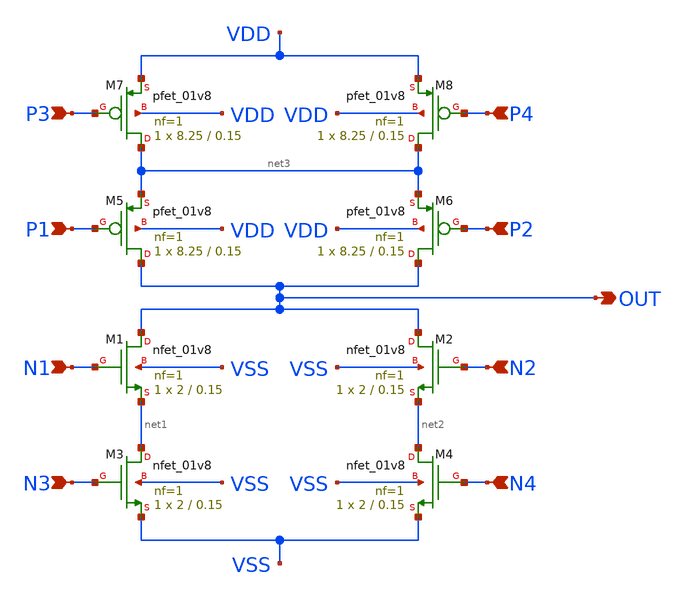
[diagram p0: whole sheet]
** sch_path: design/xschem/CG4/cg4.sch
**.subckt cg4 P3 P1 N1 N3 P4 P2 N2 N4 OUT
*.ipin P3
*.ipin P1
*.ipin N1
*.ipin N3
*.ipin P4
*.ipin P2
*.ipin N2
*.ipin N4
*.opin OUT
XM1 OUT N1 net1 VSS sky130_fd_pr__nfet_01v8 L=0.15 W=2 nf=1 ad='int((nf+1)/2) * W/nf * 0.29' as='int((nf+2)/2) * W/nf * 0.29'
+ pd='2*int((nf+1)/2) * (W/nf + 0.29)' ps='2*int((nf+2)/2) * (W/nf + 0.29)' nrd='0.29 / W' nrs='0.29 / W'
+ sa=0 sb=0 sd=0 mult=1 m=1
XM2 OUT N2 net2 VSS sky130_fd_pr__nfet_01v8 L=0.15 W=2 nf=1 ad='int((nf+1)/2) * W/nf * 0.29' as='int((nf+2)/2) * W/nf * 0.29'
+ pd='2*int((nf+1)/2) * (W/nf + 0.29)' ps='2*int((nf+2)/2) * (W/nf + 0.29)' nrd='0.29 / W' nrs='0.29 / W'
+ sa=0 sb=0 sd=0 mult=1 m=1
XM3 net1 N3 VSS VSS sky130_fd_pr__nfet_01v8 L=0.15 W=2 nf=1 ad='int((nf+1)/2) * W/nf * 0.29' as='int((nf+2)/2) * W/nf * 0.29'
+ pd='2*int((nf+1)/2) * (W/nf + 0.29)' ps='2*int((nf+2)/2) * (W/nf + 0.29)' nrd='0.29 / W' nrs='0.29 / W'
+ sa=0 sb=0 sd=0 mult=1 m=1
XM4 net2 N4 VSS VSS sky130_fd_pr__nfet_01v8 L=0.15 W=2 nf=1 ad='int((nf+1)/2) * W/nf * 0.29' as='int((nf+2)/2) * W/nf * 0.29'
+ pd='2*int((nf+1)/2) * (W/nf + 0.29)' ps='2*int((nf+2)/2) * (W/nf + 0.29)' nrd='0.29 / W' nrs='0.29 / W'
+ sa=0 sb=0 sd=0 mult=1 m=1
XM5 OUT P1 net3 VDD sky130_fd_pr__pfet_01v8 L=0.15 W=8.25 nf=1 ad='int((nf+1)/2) * W/nf * 0.29' as='int((nf+2)/2) * W/nf * 0.29'
+ pd='2*int((nf+1)/2) * (W/nf + 0.29)' ps='2*int((nf+2)/2) * (W/nf + 0.29)' nrd='0.29 / W' nrs='0.29 / W'
+ sa=0 sb=0 sd=0 mult=1 m=1
XM6 OUT P2 net3 VDD sky130_fd_pr__pfet_01v8 L=0.15 W=8.25 nf=1 ad='int((nf+1)/2) * W/nf * 0.29' as='int((nf+2)/2) * W/nf * 0.29'
+ pd='2*int((nf+1)/2) * (W/nf + 0.29)' ps='2*int((nf+2)/2) * (W/nf + 0.29)' nrd='0.29 / W' nrs='0.29 / W'
+ sa=0 sb=0 sd=0 mult=1 m=1
XM7 net3 P3 VDD VDD sky130_fd_pr__pfet_01v8 L=0.15 W=8.25 nf=1 ad='int((nf+1)/2) * W/nf * 0.29' as='int((nf+2)/2) * W/nf * 0.29'
+ pd='2*int((nf+1)/2) * (W/nf + 0.29)' ps='2*int((nf+2)/2) * (W/nf + 0.29)' nrd='0.29 / W' nrs='0.29 / W'
+ sa=0 sb=0 sd=0 mult=1 m=1
XM8 net3 P4 VDD VDD sky130_fd_pr__pfet_01v8 L=0.15 W=8.25 nf=1 ad='int((nf+1)/2) * W/nf * 0.29' as='int((nf+2)/2) * W/nf * 0.29'
+ pd='2*int((nf+1)/2) * (W/nf + 0.29)' ps='2*int((nf+2)/2) * (W/nf + 0.29)' nrd='0.29 / W' nrs='0.29 / W'
+ sa=0 sb=0 sd=0 mult=1 m=1
**.ends
.end
